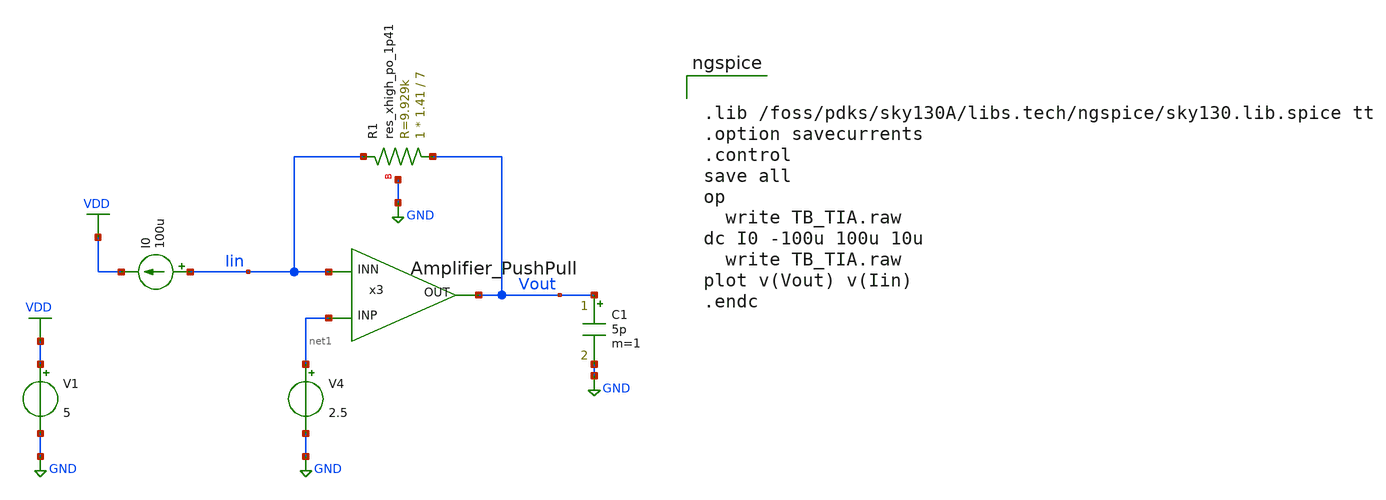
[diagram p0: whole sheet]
** sch_path: TB_TIA.sch
**.subckt TB_TIA
V1 VDD GND 5
C1 Vout GND 5p m=1
V4 net1 GND 2.5
I0 Iin VDD 100u
x3 Vout net1 Iin Amplifier_PushPull
XR1 Vout Iin GND sky130_fd_pr__res_xhigh_po_1p41 L=7 mult=1 m=1
**** begin user architecture code


.lib /foss/pdks/sky130A/libs.tech/ngspice/sky130.lib.spice tt
.option savecurrents
.control
save all
op
  write TB_TIA.raw
dc I0 -100u 100u 10u
  write TB_TIA.raw
plot v(Vout) v(Iin)
.endc


**** end user architecture code
**.ends

* expanding   symbol:  /foss/designs/Amplifier_PushPull.sym # of pins=3
** sym_path: Amplifier_PushPull.sym
** sch_path: Amplifier_PushPull.sch
.subckt Amplifier_PushPull OUT INP INN
*.ipin INN
*.opin OUT
*.ipin INP
XM1 net1 net1 GND GND sky130_fd_pr__nfet_g5v0d10v5 L=1.2 W=40 nf=4 ad='int((nf+1)/2) * W/nf * 0.29' as='int((nf+2)/2) * W/nf * 0.29'
+ pd='2*int((nf+1)/2) * (W/nf + 0.29)' ps='2*int((nf+2)/2) * (W/nf + 0.29)' nrd='0.29 / W' nrs='0.29 / W'
+ sa=0 sb=0 sd=0 mult=1 m=1
I0 VDD net1 64u
XM4 VBP VBP VDD VDD sky130_fd_pr__pfet_g5v0d10v5 L=1.2 W=48 nf=4 ad='int((nf+1)/2) * W/nf * 0.29' as='int((nf+2)/2) * W/nf * 0.29'
+ pd='2*int((nf+1)/2) * (W/nf + 0.29)' ps='2*int((nf+2)/2) * (W/nf + 0.29)' nrd='0.29 / W' nrs='0.29 / W'
+ sa=0 sb=0 sd=0 mult=1 m=1
XM5 VBP INN net3 GND sky130_fd_pr__nfet_g5v0d10v5 L=1.2 W=20 nf=2 ad='int((nf+1)/2) * W/nf * 0.29' as='int((nf+2)/2) * W/nf * 0.29'
+ pd='2*int((nf+1)/2) * (W/nf + 0.29)' ps='2*int((nf+2)/2) * (W/nf + 0.29)' nrd='0.29 / W' nrs='0.29 / W'
+ sa=0 sb=0 sd=0 mult=1 m=1
XM2 net3 net1 GND GND sky130_fd_pr__nfet_g5v0d10v5 L=1.2 W=40 nf=4 ad='int((nf+1)/2) * W/nf * 0.29' as='int((nf+2)/2) * W/nf * 0.29'
+ pd='2*int((nf+1)/2) * (W/nf + 0.29)' ps='2*int((nf+2)/2) * (W/nf + 0.29)' nrd='0.29 / W' nrs='0.29 / W'
+ sa=0 sb=0 sd=0 mult=1 m=1
XM3 net2 VBP VDD VDD sky130_fd_pr__pfet_g5v0d10v5 L=1.2 W=48 nf=4 ad='int((nf+1)/2) * W/nf * 0.29' as='int((nf+2)/2) * W/nf * 0.29'
+ pd='2*int((nf+1)/2) * (W/nf + 0.29)' ps='2*int((nf+2)/2) * (W/nf + 0.29)' nrd='0.29 / W' nrs='0.29 / W'
+ sa=0 sb=0 sd=0 mult=1 m=1
XM6 net2 INP net3 GND sky130_fd_pr__nfet_g5v0d10v5 L=1.2 W=20 nf=2 ad='int((nf+1)/2) * W/nf * 0.29' as='int((nf+2)/2) * W/nf * 0.29'
+ pd='2*int((nf+1)/2) * (W/nf + 0.29)' ps='2*int((nf+2)/2) * (W/nf + 0.29)' nrd='0.29 / W' nrs='0.29 / W'
+ sa=0 sb=0 sd=0 mult=1 m=1
XM7 net2 VBP VDD VDD sky130_fd_pr__pfet_g5v0d10v5 L=1.2 W=48 nf=4 ad='int((nf+1)/2) * W/nf * 0.29' as='int((nf+2)/2) * W/nf * 0.29'
+ pd='2*int((nf+1)/2) * (W/nf + 0.29)' ps='2*int((nf+2)/2) * (W/nf + 0.29)' nrd='0.29 / W' nrs='0.29 / W'
+ sa=0 sb=0 sd=0 mult=1 m=1
XM8 net4 VCasP net2 VDD sky130_fd_pr__pfet_g5v0d10v5 L=1.2 W=24 nf=4 ad='int((nf+1)/2) * W/nf * 0.29'
+ as='int((nf+2)/2) * W/nf * 0.29' pd='2*int((nf+1)/2) * (W/nf + 0.29)' ps='2*int((nf+2)/2) * (W/nf + 0.29)'
+ nrd='0.29 / W' nrs='0.29 / W' sa=0 sb=0 sd=0 mult=1 m=1
XM9 OUT net2 VDD VDD sky130_fd_pr__pfet_g5v0d10v5 L=1.2 W=96 nf=8 ad='int((nf+1)/2) * W/nf * 0.29' as='int((nf+2)/2) * W/nf * 0.29'
+ pd='2*int((nf+1)/2) * (W/nf + 0.29)' ps='2*int((nf+2)/2) * (W/nf + 0.29)' nrd='0.29 / W' nrs='0.29 / W'
+ sa=0 sb=0 sd=0 mult=1 m=1
XM10 net2 VCasN net4 GND sky130_fd_pr__nfet_g5v0d10v5 L=1.2 W=10 nf=2 ad='int((nf+1)/2) * W/nf * 0.29'
+ as='int((nf+2)/2) * W/nf * 0.29' pd='2*int((nf+1)/2) * (W/nf + 0.29)' ps='2*int((nf+2)/2) * (W/nf + 0.29)'
+ nrd='0.29 / W' nrs='0.29 / W' sa=0 sb=0 sd=0 mult=1 m=1
XM11 net4 net1 GND GND sky130_fd_pr__nfet_g5v0d10v5 L=1.2 W=20 nf=2 ad='int((nf+1)/2) * W/nf * 0.29'
+ as='int((nf+2)/2) * W/nf * 0.29' pd='2*int((nf+1)/2) * (W/nf + 0.29)' ps='2*int((nf+2)/2) * (W/nf + 0.29)'
+ nrd='0.29 / W' nrs='0.29 / W' sa=0 sb=0 sd=0 mult=1 m=1
XM12 OUT net4 GND GND sky130_fd_pr__nfet_g5v0d10v5 L=1.2 W=40 nf=4 ad='int((nf+1)/2) * W/nf * 0.29' as='int((nf+2)/2) * W/nf * 0.29'
+ pd='2*int((nf+1)/2) * (W/nf + 0.29)' ps='2*int((nf+2)/2) * (W/nf + 0.29)' nrd='0.29 / W' nrs='0.29 / W'
+ sa=0 sb=0 sd=0 mult=1 m=1
XR3 net5 net2 GND sky130_fd_pr__res_high_po_1p41 L=9.9 mult=1 m=1
XC1 net5 OUT sky130_fd_pr__cap_mim_m3_1 W=16 L=16 MF=4 m=4
XM16 VCasP net1 GND GND sky130_fd_pr__nfet_g5v0d10v5 L=1.2 W=20 nf=2 ad='int((nf+1)/2) * W/nf * 0.29'
+ as='int((nf+2)/2) * W/nf * 0.29' pd='2*int((nf+1)/2) * (W/nf + 0.29)' ps='2*int((nf+2)/2) * (W/nf + 0.29)'
+ nrd='0.29 / W' nrs='0.29 / W' sa=0 sb=0 sd=0 mult=1 m=1
XM17 VCasP VCasP net7 VDD sky130_fd_pr__pfet_g5v0d10v5 L=1.2 W=48 nf=4 ad='int((nf+1)/2) * W/nf * 0.29'
+ as='int((nf+2)/2) * W/nf * 0.29' pd='2*int((nf+1)/2) * (W/nf + 0.29)' ps='2*int((nf+2)/2) * (W/nf + 0.29)'
+ nrd='0.29 / W' nrs='0.29 / W' sa=0 sb=0 sd=0 mult=1 m=1
XM18 net7 net7 VDD VDD sky130_fd_pr__pfet_g5v0d10v5 L=1.2 W=48 nf=4 ad='int((nf+1)/2) * W/nf * 0.29'
+ as='int((nf+2)/2) * W/nf * 0.29' pd='2*int((nf+1)/2) * (W/nf + 0.29)' ps='2*int((nf+2)/2) * (W/nf + 0.29)'
+ nrd='0.29 / W' nrs='0.29 / W' sa=0 sb=0 sd=0 mult=1 m=1
XM19 net6 net6 GND GND sky130_fd_pr__nfet_g5v0d10v5 L=1.2 W=20 nf=2 ad='int((nf+1)/2) * W/nf * 0.29'
+ as='int((nf+2)/2) * W/nf * 0.29' pd='2*int((nf+1)/2) * (W/nf + 0.29)' ps='2*int((nf+2)/2) * (W/nf + 0.29)'
+ nrd='0.29 / W' nrs='0.29 / W' sa=0 sb=0 sd=0 mult=1 m=1
XM20 VCasN VCasN net6 GND sky130_fd_pr__nfet_g5v0d10v5 L=1.2 W=20 nf=2 ad='int((nf+1)/2) * W/nf * 0.29'
+ as='int((nf+2)/2) * W/nf * 0.29' pd='2*int((nf+1)/2) * (W/nf + 0.29)' ps='2*int((nf+2)/2) * (W/nf + 0.29)'
+ nrd='0.29 / W' nrs='0.29 / W' sa=0 sb=0 sd=0 mult=1 m=1
XM21 VCasN VBP VDD VDD sky130_fd_pr__pfet_g5v0d10v5 L=1.2 W=48 nf=4 ad='int((nf+1)/2) * W/nf * 0.29'
+ as='int((nf+2)/2) * W/nf * 0.29' pd='2*int((nf+1)/2) * (W/nf + 0.29)' ps='2*int((nf+2)/2) * (W/nf + 0.29)'
+ nrd='0.29 / W' nrs='0.29 / W' sa=0 sb=0 sd=0 mult=1 m=1
.ends

.GLOBAL VDD
.GLOBAL GND
.end
